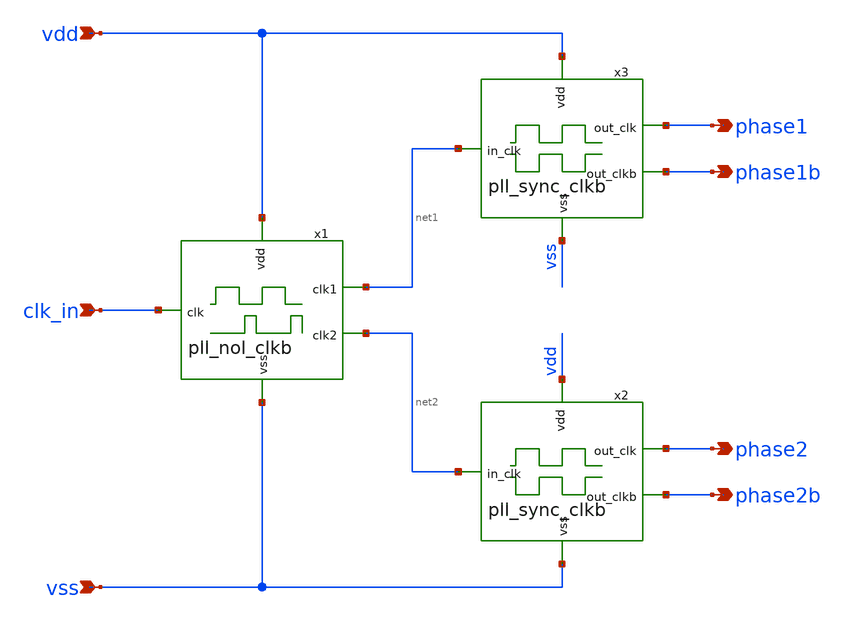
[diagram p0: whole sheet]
** sch_path: pll/pll_cp_sw_clk_gen/xschem/pll_cp_sw_clk_gen.sch
**.subckt pll_cp_sw_clk_gen vdd vss clk_in phase1 phase1b phase2 phase2b
*.ipin vdd
*.ipin vss
*.ipin clk_in
*.opin phase1
*.opin phase1b
*.opin phase2
*.opin phase2b
x1 net1 vdd vss clk_in net2 pll_nol_clkb
x2 phase2 vdd vss net2 phase2b pll_sync_clkb
x3 phase1 vdd vss net1 phase1b pll_sync_clkb
**.ends

* expanding   symbol:  pll_nol_clkb/xschem/pll_nol_clkb.sym # of pins=5
** sym_path: pll/pll_nol_clkb/xschem/pll_nol_clkb.sym
** sch_path: pll/pll_nol_clkb/xschem/pll_nol_clkb.sch
.subckt pll_nol_clkb clk1 vdd vss clk clk2
*.opin clk1
*.opin clk2
*.ipin vdd
*.ipin vss
*.ipin clk
**** begin user architecture code
* .include $::SKYWATER_STDCELLS/cells/
.include $::SKYWATER_STDCELLS/cells/and2/sky130_fd_sc_hd__and2_1.spice
.include $::SKYWATER_STDCELLS/cells/and2/sky130_fd_sc_hd__and2_2.spice
.include $::SKYWATER_STDCELLS_HS/cells/and2/sky130_fd_sc_hs__and2_1.spice
.include $::SKYWATER_STDCELLS_HS/cells/and2/sky130_fd_sc_hs__and2_2.spice

.include $::SKYWATER_STDCELLS/cells/nand2/sky130_fd_sc_hd__nand2_1.spice
.include $::SKYWATER_STDCELLS/cells/nand2/sky130_fd_sc_hd__nand2_2.spice
.include $::SKYWATER_STDCELLS_HS/cells/nand2/sky130_fd_sc_hs__nand2_1.spice
.include $::SKYWATER_STDCELLS_HS/cells/nand2/sky130_fd_sc_hs__nand2_2.spice

.include $::SKYWATER_STDCELLS/cells/or2/sky130_fd_sc_hd__or2_1.spice
.include $::SKYWATER_STDCELLS/cells/or2/sky130_fd_sc_hd__or2_2.spice
.include $::SKYWATER_STDCELLS_HS/cells/or2/sky130_fd_sc_hs__or2_1.spice
.include $::SKYWATER_STDCELLS_HS/cells/or2/sky130_fd_sc_hs__or2_2.spice

.include $::SKYWATER_STDCELLS/cells/buf/sky130_fd_sc_hd__buf_1.spice
.include $::SKYWATER_STDCELLS_HS/cells/buf/sky130_fd_sc_hs__buf_1.spice

.include $::SKYWATER_STDCELLS/cells/dfrbp/sky130_fd_sc_hd__dfrbp_1.spice
.include $::SKYWATER_STDCELLS/cells/dfrbp/sky130_fd_sc_hd__dfrbp_2.spice
.include $::SKYWATER_STDCELLS_HS/cells/dfrbp/sky130_fd_sc_hs__dfrbp_1.spice
.include $::SKYWATER_STDCELLS_HS/cells/dfrbp/sky130_fd_sc_hs__dfrbp_2.spice

.include $::SKYWATER_STDCELLS/cells/inv/sky130_fd_sc_hd__inv_1.spice
.include $::SKYWATER_STDCELLS/cells/inv/sky130_fd_sc_hd__inv_2.spice
.include $::SKYWATER_STDCELLS/cells/inv/sky130_fd_sc_hd__inv_4.spice
.include $::SKYWATER_STDCELLS/cells/inv/sky130_fd_sc_hd__inv_8.spice
.include $::SKYWATER_STDCELLS/cells/inv/sky130_fd_sc_hd__inv_16.spice
.include $::SKYWATER_STDCELLS_HS/cells/inv/sky130_fd_sc_hs__inv_1.spice
.include $::SKYWATER_STDCELLS_HS/cells/inv/sky130_fd_sc_hs__inv_2.spice
.include $::SKYWATER_STDCELLS_HS/cells/inv/sky130_fd_sc_hs__inv_4.spice
.include $::SKYWATER_STDCELLS_HS/cells/inv/sky130_fd_sc_hs__inv_8.spice
.include $::SKYWATER_STDCELLS_HS/cells/inv/sky130_fd_sc_hs__inv_16.spice

.include $::SKYWATER_STDCELLS/cells/mux2/sky130_fd_sc_hd__mux2_2.spice
.include $::SKYWATER_STDCELLS/cells/nand2/sky130_fd_sc_hd__nand2_1.spice

.include $::SKYWATER_STDCELLS/cells/tap/sky130_fd_sc_hd__tap_2.spice
.include $::SKYWATER_STDCELLS/cells/tapvpwrvgnd/sky130_fd_sc_hd__tapvpwrvgnd_1.spice

**** end user architecture code
x3 clk1b vss vss vdd vdd clk1 sky130_fd_sc_hd__inv_1
x4 clk1 vss vss vdd vdd clk1fb sky130_fd_sc_hd__inv_1
x5 clk2b vss vss vdd vdd clk2 sky130_fd_sc_hd__inv_1
x6 clk2 vss vss vdd vdd clk2fb sky130_fd_sc_hd__inv_1
x7 clk vss vss vdd vdd clkb sky130_fd_sc_hd__inv_1
x1 clkb clk2fb vss vss vdd vdd clk1b sky130_fd_sc_hd__nand2_2
x2 clk1fb clk vss vss vdd vdd clk2b sky130_fd_sc_hd__nand2_2
* noconn vdd
* noconn vss
.ends


* expanding   symbol:  pll_sync_clkb/xschem/pll_sync_clkb.sym # of pins=5
** sym_path: pll/pll_sync_clkb/xschem/pll_sync_clkb.sym
** sch_path: pll/pll_sync_clkb/xschem/pll_sync_clkb.sch
.subckt pll_sync_clkb out_clk vdd vss in_clk out_clkb
*.opin out_clk
*.opin out_clkb
*.ipin vdd
*.ipin vss
*.ipin in_clk
**** begin user architecture code
* .include $::SKYWATER_STDCELLS/cells/
.include $::SKYWATER_STDCELLS/cells/and2/sky130_fd_sc_hd__and2_1.spice
.include $::SKYWATER_STDCELLS/cells/and2/sky130_fd_sc_hd__and2_2.spice
.include $::SKYWATER_STDCELLS_HS/cells/and2/sky130_fd_sc_hs__and2_1.spice
.include $::SKYWATER_STDCELLS_HS/cells/and2/sky130_fd_sc_hs__and2_2.spice

.include $::SKYWATER_STDCELLS/cells/nand2/sky130_fd_sc_hd__nand2_1.spice
.include $::SKYWATER_STDCELLS/cells/nand2/sky130_fd_sc_hd__nand2_2.spice
.include $::SKYWATER_STDCELLS_HS/cells/nand2/sky130_fd_sc_hs__nand2_1.spice
.include $::SKYWATER_STDCELLS_HS/cells/nand2/sky130_fd_sc_hs__nand2_2.spice

.include $::SKYWATER_STDCELLS/cells/or2/sky130_fd_sc_hd__or2_1.spice
.include $::SKYWATER_STDCELLS/cells/or2/sky130_fd_sc_hd__or2_2.spice
.include $::SKYWATER_STDCELLS_HS/cells/or2/sky130_fd_sc_hs__or2_1.spice
.include $::SKYWATER_STDCELLS_HS/cells/or2/sky130_fd_sc_hs__or2_2.spice

.include $::SKYWATER_STDCELLS/cells/buf/sky130_fd_sc_hd__buf_1.spice
.include $::SKYWATER_STDCELLS_HS/cells/buf/sky130_fd_sc_hs__buf_1.spice

.include $::SKYWATER_STDCELLS/cells/dfrbp/sky130_fd_sc_hd__dfrbp_1.spice
.include $::SKYWATER_STDCELLS/cells/dfrbp/sky130_fd_sc_hd__dfrbp_2.spice
.include $::SKYWATER_STDCELLS_HS/cells/dfrbp/sky130_fd_sc_hs__dfrbp_1.spice
.include $::SKYWATER_STDCELLS_HS/cells/dfrbp/sky130_fd_sc_hs__dfrbp_2.spice

.include $::SKYWATER_STDCELLS/cells/inv/sky130_fd_sc_hd__inv_1.spice
.include $::SKYWATER_STDCELLS/cells/inv/sky130_fd_sc_hd__inv_2.spice
.include $::SKYWATER_STDCELLS/cells/inv/sky130_fd_sc_hd__inv_4.spice
.include $::SKYWATER_STDCELLS/cells/inv/sky130_fd_sc_hd__inv_8.spice
.include $::SKYWATER_STDCELLS/cells/inv/sky130_fd_sc_hd__inv_16.spice
.include $::SKYWATER_STDCELLS_HS/cells/inv/sky130_fd_sc_hs__inv_1.spice
.include $::SKYWATER_STDCELLS_HS/cells/inv/sky130_fd_sc_hs__inv_2.spice
.include $::SKYWATER_STDCELLS_HS/cells/inv/sky130_fd_sc_hs__inv_4.spice
.include $::SKYWATER_STDCELLS_HS/cells/inv/sky130_fd_sc_hs__inv_8.spice
.include $::SKYWATER_STDCELLS_HS/cells/inv/sky130_fd_sc_hs__inv_16.spice

.include $::SKYWATER_STDCELLS/cells/mux2/sky130_fd_sc_hd__mux2_2.spice
.include $::SKYWATER_STDCELLS/cells/nand2/sky130_fd_sc_hd__nand2_1.spice

.include $::SKYWATER_STDCELLS/cells/tap/sky130_fd_sc_hd__tap_2.spice
.include $::SKYWATER_STDCELLS/cells/tapvpwrvgnd/sky130_fd_sc_hd__tapvpwrvgnd_1.spice

**** end user architecture code
x1 in_clk vss vss vdd vdd net1 sky130_fd_sc_hd__inv_2
x2 net1 vss vss vdd vdd net2 sky130_fd_sc_hd__inv_2
x4 stor_node vss vss vdd vdd out_clk sky130_fd_sc_hd__inv_1
x6 stor_node_b vss vss vdd vdd out_clkb sky130_fd_sc_hd__inv_1
x7 stor_node_b vss vss vdd vdd stor_node sky130_fd_sc_hd__inv_2
x9 stor_node vss vss vdd vdd stor_node_b sky130_fd_sc_hd__inv_2
x3 net2 vss vss vdd vdd stor_node sky130_fd_sc_hd__inv_1
x5 net1 vss vss vdd vdd stor_node_b sky130_fd_sc_hd__inv_1
* noconn vdd
* noconn vss
.ends

.end
